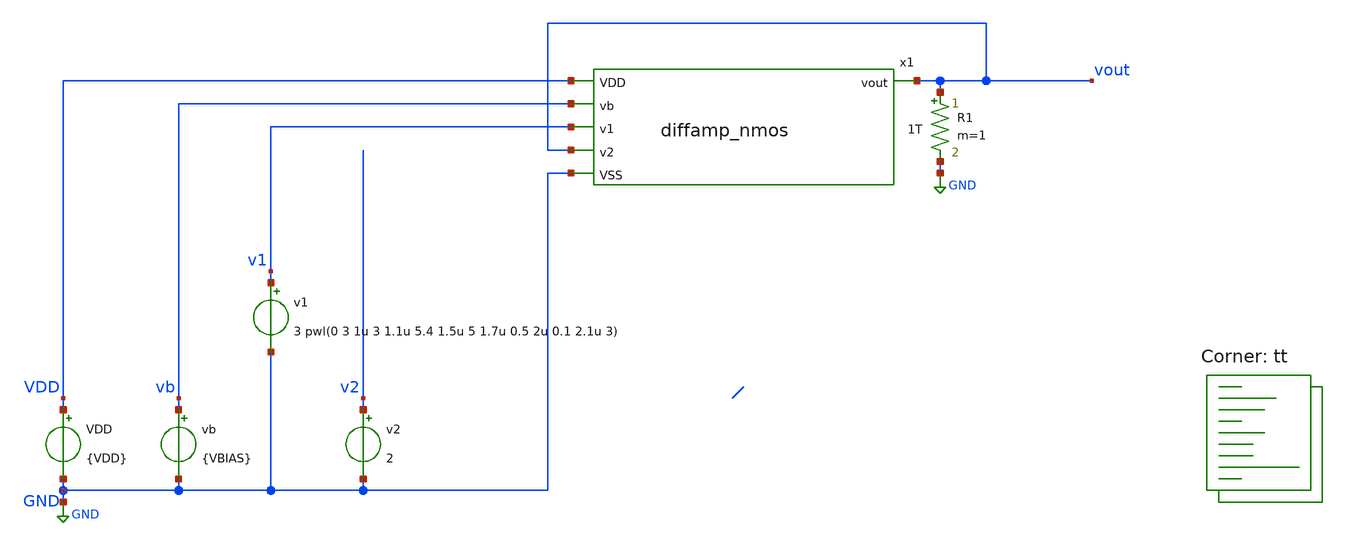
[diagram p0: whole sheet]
** sch_path: xschem/test_diffamp_nmos.sch
**.subckt test_diffamp_nmos
x1 VDD vb vout v1 vout GND diffamp_nmos
VDD VDD GND {VDD}
vb vb GND {VBIAS}
v1 v1 GND 3 pwl(0 3 1u 3 1.1u 5.4 1.5u 5 1.7u 0.5 2u 0.1 2.1u 3)
v2 v2 GND 2
R1 vout GND 1T m=1
**** begin user architecture code
.lib $::SKYWATER_MODELS/sky130.lib.spice tt



.options reltol=0.0001 abstol=10e-15
*.include diffamp_nmos.spice
.param VDD=6
.param VSS=0
.param VBIAS=1
.options savecurrents
* .options reltol=0.01 abstol=10e-12
.control
  save all
  op
  remzerovec
  write test_diffamp_nmos.raw
  set appendwrite
  * vb sweep
  dc v1 0 6 0.2 vb 0 6 1
  remzerovec
  write test_diffamp_nmos.raw
  * dc sweep
  dc v1 0 6 0.1
  remzerovec
  write test_diffamp_nmos.raw
  * tran
  tran 1n 3u
  remzerovec
  write test_diffamp_nmos.raw
.endc



**** end user architecture code
**.ends

* expanding   symbol:  diffamp_nmos.sym # of pins=6
** sym_path: xschem/diffamp_nmos.sym
** sch_path: xschem/diffamp_nmos.sch
.subckt diffamp_nmos VDD vb vout v1 v2 VSS
*.ipin v1
*.ipin v2
*.ipin VSS
*.ipin VDD
*.ipin vb
*.opin vout
XM1 int4 v1 int1 VSS sky130_fd_pr__nfet_g5v0d10v5 L=1.5 W=1 nf=1 ad='int((nf+1)/2) * W/nf * 0.29' as='int((nf+2)/2) * W/nf * 0.29'
+ pd='2*int((nf+1)/2) * (W/nf + 0.29)' ps='2*int((nf+2)/2) * (W/nf + 0.29)' nrd='0.29 / W' nrs='0.29 / W'
+ sa=0 sb=0 sd=0 mult=1 m=1
XM2 int3 v2 int1 VSS sky130_fd_pr__nfet_g5v0d10v5 L=1.5 W=1 nf=1 ad='int((nf+1)/2) * W/nf * 0.29' as='int((nf+2)/2) * W/nf * 0.29'
+ pd='2*int((nf+1)/2) * (W/nf + 0.29)' ps='2*int((nf+2)/2) * (W/nf + 0.29)' nrd='0.29 / W' nrs='0.29 / W'
+ sa=0 sb=0 sd=0 mult=1 m=1
XM3a int1 vb int5 VSS sky130_fd_pr__nfet_g5v0d10v5 L=1.5 W=1 nf=1 ad='int((nf+1)/2) * W/nf * 0.29' as='int((nf+2)/2) * W/nf * 0.29'
+ pd='2*int((nf+1)/2) * (W/nf + 0.29)' ps='2*int((nf+2)/2) * (W/nf + 0.29)' nrd='0.29 / W' nrs='0.29 / W'
+ sa=0 sb=0 sd=0 mult=1 m=1
XM4 int4 int4 VDD VDD sky130_fd_pr__pfet_g5v0d10v5 L=1.5 W=1 nf=1 ad='int((nf+1)/2) * W/nf * 0.29' as='int((nf+2)/2) * W/nf * 0.29'
+ pd='2*int((nf+1)/2) * (W/nf + 0.29)' ps='2*int((nf+2)/2) * (W/nf + 0.29)' nrd='0.29 / W' nrs='0.29 / W'
+ sa=0 sb=0 sd=0 mult=1 m=1
XM5 vout int4 VDD VDD sky130_fd_pr__pfet_g5v0d10v5 L=1.5 W=1 nf=1 ad='int((nf+1)/2) * W/nf * 0.29' as='int((nf+2)/2) * W/nf * 0.29'
+ pd='2*int((nf+1)/2) * (W/nf + 0.29)' ps='2*int((nf+2)/2) * (W/nf + 0.29)' nrd='0.29 / W' nrs='0.29 / W'
+ sa=0 sb=0 sd=0 mult=1 m=1
XM6 int3 int3 VDD VDD sky130_fd_pr__pfet_g5v0d10v5 L=1.5 W=1 nf=1 ad='int((nf+1)/2) * W/nf * 0.29' as='int((nf+2)/2) * W/nf * 0.29'
+ pd='2*int((nf+1)/2) * (W/nf + 0.29)' ps='2*int((nf+2)/2) * (W/nf + 0.29)' nrd='0.29 / W' nrs='0.29 / W'
+ sa=0 sb=0 sd=0 mult=1 m=1
XM7 int2 int3 VDD VDD sky130_fd_pr__pfet_g5v0d10v5 L=1.5 W=1 nf=1 ad='int((nf+1)/2) * W/nf * 0.29' as='int((nf+2)/2) * W/nf * 0.29'
+ pd='2*int((nf+1)/2) * (W/nf + 0.29)' ps='2*int((nf+2)/2) * (W/nf + 0.29)' nrd='0.29 / W' nrs='0.29 / W'
+ sa=0 sb=0 sd=0 mult=1 m=1
XM8 int2 int2 VSS VSS sky130_fd_pr__nfet_g5v0d10v5 L=1.5 W=1 nf=1 ad='int((nf+1)/2) * W/nf * 0.29' as='int((nf+2)/2) * W/nf * 0.29'
+ pd='2*int((nf+1)/2) * (W/nf + 0.29)' ps='2*int((nf+2)/2) * (W/nf + 0.29)' nrd='0.29 / W' nrs='0.29 / W'
+ sa=0 sb=0 sd=0 mult=1 m=1
XM9 vout int2 VSS VSS sky130_fd_pr__nfet_g5v0d10v5 L=1.5 W=1 nf=1 ad='int((nf+1)/2) * W/nf * 0.29' as='int((nf+2)/2) * W/nf * 0.29'
+ pd='2*int((nf+1)/2) * (W/nf + 0.29)' ps='2*int((nf+2)/2) * (W/nf + 0.29)' nrd='0.29 / W' nrs='0.29 / W'
+ sa=0 sb=0 sd=0 mult=1 m=1
XM3b int5 vb VSS VSS sky130_fd_pr__nfet_g5v0d10v5 L=1.5 W=1 nf=1 ad='int((nf+1)/2) * W/nf * 0.29' as='int((nf+2)/2) * W/nf * 0.29'
+ pd='2*int((nf+1)/2) * (W/nf + 0.29)' ps='2*int((nf+2)/2) * (W/nf + 0.29)' nrd='0.29 / W' nrs='0.29 / W'
+ sa=0 sb=0 sd=0 mult=1 m=1
.save v(int1)
.save v(int2)
.save v(int3)
.save v(int4)
.ends

.GLOBAL GND
.end
